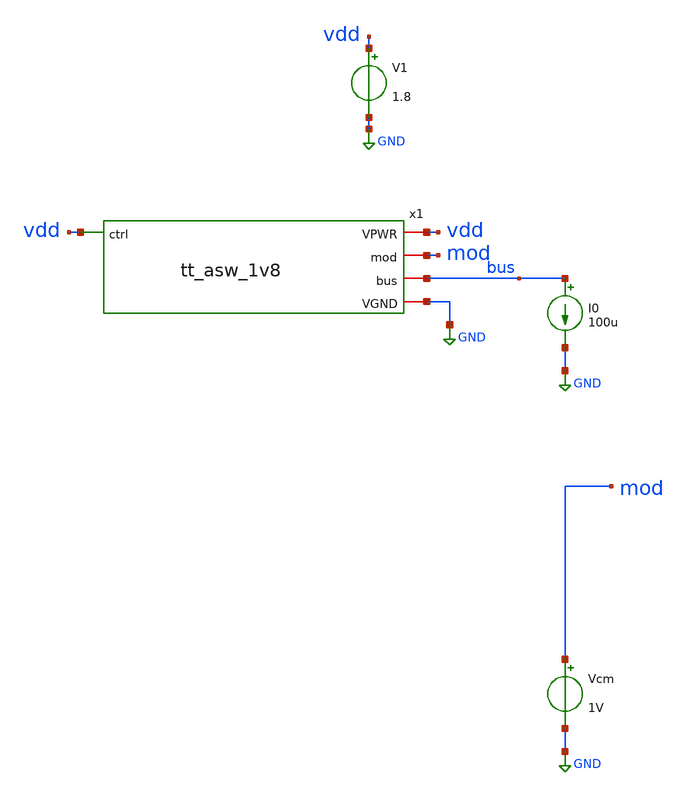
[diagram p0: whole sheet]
** sch_path: asw/sky130/tt_asw_1v8/xschem/tb_rdson.sch
**.subckt tb_rdson
x1 GND vdd vdd mod bus tt_asw_1v8
V1 vdd GND 1.8
Vcm mod GND 1V
I0 bus GND 100u
**** begin user architecture code

** opencircuitdesign pdks install
.lib $::SKYWATER_MODELS/sky130.lib.spice tt
.include $::SKYWATER_STDCELLS/sky130_fd_sc_hd.spice





.param mc_mm_switch=0
.control
dc Vcm 0 1.8 0.01
plot (v(mod) - v(bus)) / 100u
write tb_rdson.raw
*quit 0
.endc
.end


**** end user architecture code
**.ends

* expanding   symbol:  tt_asw_1v8.sym # of pins=5
** sym_path: asw/sky130/tt_asw_1v8/xschem/tt_asw_1v8.sym
** sch_path: asw/sky130/tt_asw_1v8/xschem/tt_asw_1v8.sch
.subckt tt_asw_1v8 VGND VPWR ctrl mod bus
*.iopin VPWR
*.iopin VGND
*.iopin mod
*.iopin bus
*.ipin ctrl
XM4 tgon tgon_n VGND VGND sky130_fd_pr__nfet_01v8 L=0.15 W=1.5 nf=1 ad='int((nf+1)/2) * W/nf * 0.29'
+ as='int((nf+2)/2) * W/nf * 0.29' pd='2*int((nf+1)/2) * (W/nf + 0.29)' ps='2*int((nf+2)/2) * (W/nf + 0.29)'
+ nrd='0.29 / W' nrs='0.29 / W' sa=0 sb=0 sd=0 mult=1 m=1
XM3 tgon tgon_n VPWR VPWR sky130_fd_pr__pfet_01v8 L=0.15 W=3 nf=2 ad='int((nf+1)/2) * W/nf * 0.29' as='int((nf+2)/2) * W/nf * 0.29'
+ pd='2*int((nf+1)/2) * (W/nf + 0.29)' ps='2*int((nf+2)/2) * (W/nf + 0.29)' nrd='0.29 / W' nrs='0.29 / W'
+ sa=0 sb=0 sd=0 mult=1 m=1
XM2 tgon_n ctrl VGND VGND sky130_fd_pr__nfet_01v8 L=0.15 W=1.5 nf=1 ad='int((nf+1)/2) * W/nf * 0.29'
+ as='int((nf+2)/2) * W/nf * 0.29' pd='2*int((nf+1)/2) * (W/nf + 0.29)' ps='2*int((nf+2)/2) * (W/nf + 0.29)'
+ nrd='0.29 / W' nrs='0.29 / W' sa=0 sb=0 sd=0 mult=1 m=1
XM1 tgon_n ctrl VPWR VPWR sky130_fd_pr__pfet_01v8 L=0.15 W=3 nf=2 ad='int((nf+1)/2) * W/nf * 0.29' as='int((nf+2)/2) * W/nf * 0.29'
+ pd='2*int((nf+1)/2) * (W/nf + 0.29)' ps='2*int((nf+2)/2) * (W/nf + 0.29)' nrd='0.29 / W' nrs='0.29 / W'
+ sa=0 sb=0 sd=0 mult=1 m=1
XM6 bus tgon mod VGND sky130_fd_pr__nfet_01v8_lvt L=0.35 W=31.5 nf=7 ad='int((nf+1)/2) * W/nf * 0.29'
+ as='int((nf+2)/2) * W/nf * 0.29' pd='2*int((nf+1)/2) * (W/nf + 0.29)' ps='2*int((nf+2)/2) * (W/nf + 0.29)'
+ nrd='0.29 / W' nrs='0.29 / W' sa=0 sb=0 sd=0 mult=1 m=1
XM5 bus tgon_n mod VPWR sky130_fd_pr__pfet_01v8_lvt L=0.35 W=94.5 nf=21 ad='int((nf+1)/2) * W/nf * 0.29'
+ as='int((nf+2)/2) * W/nf * 0.29' pd='2*int((nf+1)/2) * (W/nf + 0.29)' ps='2*int((nf+2)/2) * (W/nf + 0.29)'
+ nrd='0.29 / W' nrs='0.29 / W' sa=0 sb=0 sd=0 mult=1 m=1
.ends

.GLOBAL GND
.end
